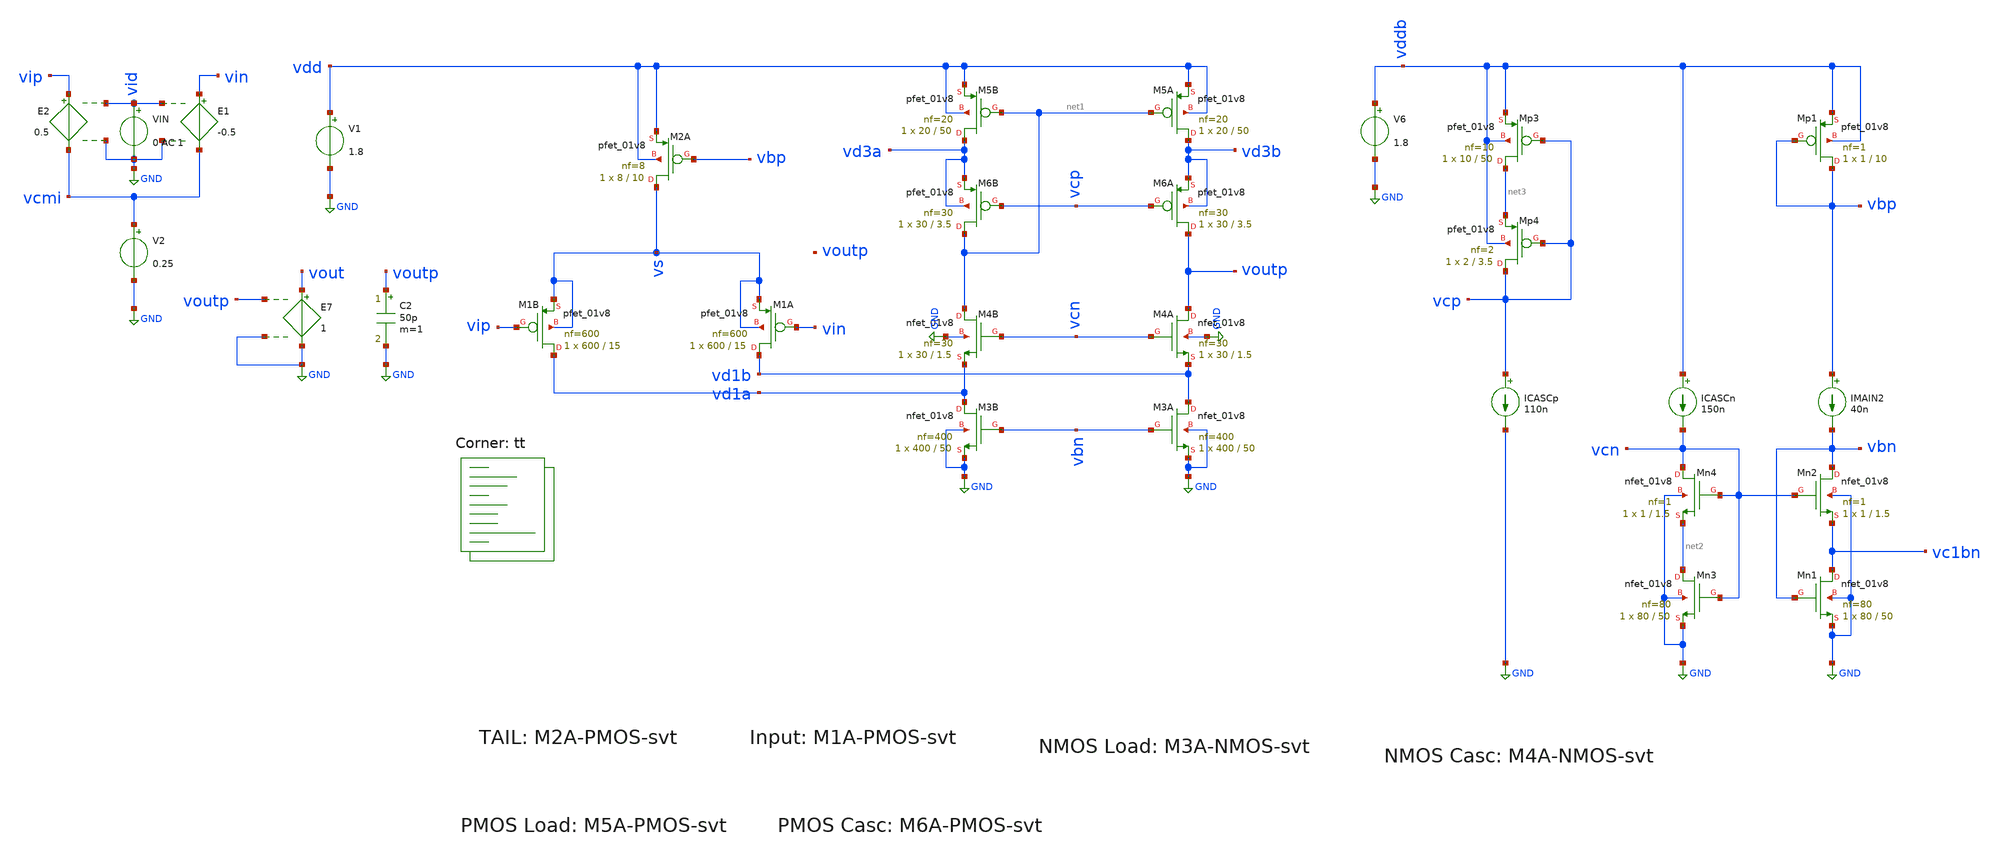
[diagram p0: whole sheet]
** sch_path: circuit-level/xschem/aux-amp/ota_gm_boost_1.sch
**.subckt ota_gm_boost_1
V1 vdd GND 1.8
V2 vcmi GND 0.25
E1 vin vcmi vid GND -0.5
E2 vip vcmi vid GND 0.5
VIN vid GND 0 AC 1
E7 vout GND voutp GND 1
XM2A vs vbp vdd vdd sky130_fd_pr__pfet_01v8 L=10 W=8 nf=8 ad='int((nf+1)/2) * W/nf * 0.29' as='int((nf+2)/2) * W/nf * 0.29'
+ pd='2*int((nf+1)/2) * (W/nf + 0.29)' ps='2*int((nf+2)/2) * (W/nf + 0.29)' nrd='0.29 / W' nrs='0.29 / W'
+ sa=0 sb=0 sd=0 mult=1 m=1
XM1B vd1a vip vs vs sky130_fd_pr__pfet_01v8 L=15 W=600 nf=600 ad='int((nf+1)/2) * W/nf * 0.29' as='int((nf+2)/2) * W/nf * 0.29'
+ pd='2*int((nf+1)/2) * (W/nf + 0.29)' ps='2*int((nf+2)/2) * (W/nf + 0.29)' nrd='0.29 / W' nrs='0.29 / W'
+ sa=0 sb=0 sd=0 mult=1 m=1
XM1A vd1b vin vs vs sky130_fd_pr__pfet_01v8 L=15 W=600 nf=600 ad='int((nf+1)/2) * W/nf * 0.29' as='int((nf+2)/2) * W/nf * 0.29'
+ pd='2*int((nf+1)/2) * (W/nf + 0.29)' ps='2*int((nf+2)/2) * (W/nf + 0.29)' nrd='0.29 / W' nrs='0.29 / W'
+ sa=0 sb=0 sd=0 mult=1 m=1
XM4B net1 vcn vd1a GND sky130_fd_pr__nfet_01v8 L=1.5 W=30 nf=30 ad='int((nf+1)/2) * W/nf * 0.29' as='int((nf+2)/2) * W/nf * 0.29'
+ pd='2*int((nf+1)/2) * (W/nf + 0.29)' ps='2*int((nf+2)/2) * (W/nf + 0.29)' nrd='0.29 / W' nrs='0.29 / W'
+ sa=0 sb=0 sd=0 mult=1 m=1
XM4A voutp vcn vd1b GND sky130_fd_pr__nfet_01v8 L=1.5 W=30 nf=30 ad='int((nf+1)/2) * W/nf * 0.29' as='int((nf+2)/2) * W/nf * 0.29'
+ pd='2*int((nf+1)/2) * (W/nf + 0.29)' ps='2*int((nf+2)/2) * (W/nf + 0.29)' nrd='0.29 / W' nrs='0.29 / W'
+ sa=0 sb=0 sd=0 mult=1 m=1
XM3B vd1a vbn GND GND sky130_fd_pr__nfet_01v8 L=50 W=400 nf=400 ad='int((nf+1)/2) * W/nf * 0.29' as='int((nf+2)/2) * W/nf * 0.29'
+ pd='2*int((nf+1)/2) * (W/nf + 0.29)' ps='2*int((nf+2)/2) * (W/nf + 0.29)' nrd='0.29 / W' nrs='0.29 / W'
+ sa=0 sb=0 sd=0 mult=1 m=1
XM3A vd1b vbn GND GND sky130_fd_pr__nfet_01v8 L=50 W=400 nf=400 ad='int((nf+1)/2) * W/nf * 0.29' as='int((nf+2)/2) * W/nf * 0.29'
+ pd='2*int((nf+1)/2) * (W/nf + 0.29)' ps='2*int((nf+2)/2) * (W/nf + 0.29)' nrd='0.29 / W' nrs='0.29 / W'
+ sa=0 sb=0 sd=0 mult=1 m=1
XM5B vd3a net1 vdd vdd sky130_fd_pr__pfet_01v8 L=50 W=20 nf=20 ad='int((nf+1)/2) * W/nf * 0.29' as='int((nf+2)/2) * W/nf * 0.29'
+ pd='2*int((nf+1)/2) * (W/nf + 0.29)' ps='2*int((nf+2)/2) * (W/nf + 0.29)' nrd='0.29 / W' nrs='0.29 / W'
+ sa=0 sb=0 sd=0 mult=1 m=1
XM5A vd3b net1 vdd vdd sky130_fd_pr__pfet_01v8 L=50 W=20 nf=20 ad='int((nf+1)/2) * W/nf * 0.29' as='int((nf+2)/2) * W/nf * 0.29'
+ pd='2*int((nf+1)/2) * (W/nf + 0.29)' ps='2*int((nf+2)/2) * (W/nf + 0.29)' nrd='0.29 / W' nrs='0.29 / W'
+ sa=0 sb=0 sd=0 mult=1 m=1
C2 voutp GND 50p m=1
XM6B net1 vcp vd3a vd3a sky130_fd_pr__pfet_01v8 L=3.5 W=30 nf=30 ad='int((nf+1)/2) * W/nf * 0.29' as='int((nf+2)/2) * W/nf * 0.29'
+ pd='2*int((nf+1)/2) * (W/nf + 0.29)' ps='2*int((nf+2)/2) * (W/nf + 0.29)' nrd='0.29 / W' nrs='0.29 / W'
+ sa=0 sb=0 sd=0 mult=1 m=1
XM6A voutp vcp vd3b vd3b sky130_fd_pr__pfet_01v8 L=3.5 W=30 nf=30 ad='int((nf+1)/2) * W/nf * 0.29' as='int((nf+2)/2) * W/nf * 0.29'
+ pd='2*int((nf+1)/2) * (W/nf + 0.29)' ps='2*int((nf+2)/2) * (W/nf + 0.29)' nrd='0.29 / W' nrs='0.29 / W'
+ sa=0 sb=0 sd=0 mult=1 m=1
V6 vddb GND 1.8
XMn2 vbn vcn vc1bn GND sky130_fd_pr__nfet_01v8 L=1.5 W=1 nf=1 ad='int((nf+1)/2) * W/nf * 0.29' as='int((nf+2)/2) * W/nf * 0.29'
+ pd='2*int((nf+1)/2) * (W/nf + 0.29)' ps='2*int((nf+2)/2) * (W/nf + 0.29)' nrd='0.29 / W' nrs='0.29 / W'
+ sa=0 sb=0 sd=0 mult=1 m=1
XMn4 vcn vcn net2 GND sky130_fd_pr__nfet_01v8 L=1.5 W=1 nf=1 ad='int((nf+1)/2) * W/nf * 0.29' as='int((nf+2)/2) * W/nf * 0.29'
+ pd='2*int((nf+1)/2) * (W/nf + 0.29)' ps='2*int((nf+2)/2) * (W/nf + 0.29)' nrd='0.29 / W' nrs='0.29 / W'
+ sa=0 sb=0 sd=0 mult=1 m=1
ICASCn vddb vcn 150n
XMn1 vc1bn vbn GND GND sky130_fd_pr__nfet_01v8 L=50 W=80 nf=80 ad='int((nf+1)/2) * W/nf * 0.29' as='int((nf+2)/2) * W/nf * 0.29'
+ pd='2*int((nf+1)/2) * (W/nf + 0.29)' ps='2*int((nf+2)/2) * (W/nf + 0.29)' nrd='0.29 / W' nrs='0.29 / W'
+ sa=0 sb=0 sd=0 mult=1 m=1
IMAIN2 vbp vbn 40n
XMn3 net2 vcn GND GND sky130_fd_pr__nfet_01v8 L=50 W=80 nf=80 ad='int((nf+1)/2) * W/nf * 0.29' as='int((nf+2)/2) * W/nf * 0.29'
+ pd='2*int((nf+1)/2) * (W/nf + 0.29)' ps='2*int((nf+2)/2) * (W/nf + 0.29)' nrd='0.29 / W' nrs='0.29 / W'
+ sa=0 sb=0 sd=0 mult=1 m=1
XMp1 vbp vbp vddb vddb sky130_fd_pr__pfet_01v8 L=10 W=1 nf=1 ad='int((nf+1)/2) * W/nf * 0.29' as='int((nf+2)/2) * W/nf * 0.29'
+ pd='2*int((nf+1)/2) * (W/nf + 0.29)' ps='2*int((nf+2)/2) * (W/nf + 0.29)' nrd='0.29 / W' nrs='0.29 / W'
+ sa=0 sb=0 sd=0 mult=1 m=1
ICASCp vcp GND 110n
XMp3 net3 vcp vddb vddb sky130_fd_pr__pfet_01v8 L=50 W=10 nf=10 ad='int((nf+1)/2) * W/nf * 0.29' as='int((nf+2)/2) * W/nf * 0.29'
+ pd='2*int((nf+1)/2) * (W/nf + 0.29)' ps='2*int((nf+2)/2) * (W/nf + 0.29)' nrd='0.29 / W' nrs='0.29 / W'
+ sa=0 sb=0 sd=0 mult=1 m=1
XMp4 vcp vcp net3 vddb sky130_fd_pr__pfet_01v8 L=3.5 W=2 nf=2 ad='int((nf+1)/2) * W/nf * 0.29' as='int((nf+2)/2) * W/nf * 0.29'
+ pd='2*int((nf+1)/2) * (W/nf + 0.29)' ps='2*int((nf+2)/2) * (W/nf + 0.29)' nrd='0.29 / W' nrs='0.29 / W'
+ sa=0 sb=0 sd=0 mult=1 m=1
**** begin user architecture code
.lib $::SKYWATER_MODELS/sky130.lib.spice tt


.control

save @m.xm1a.msky130_fd_pr__pfet_01v8[id]
save @m.xm1a.msky130_fd_pr__pfet_01v8[vth]
save @m.xm1a.msky130_fd_pr__pfet_01v8[vgs]
save @m.xm1a.msky130_fd_pr__pfet_01v8[vds]
save @m.xm1a.msky130_fd_pr__pfet_01v8[vdsat]
save @m.xm1a.msky130_fd_pr__pfet_01v8[gm]
save @m.xm1a.msky130_fd_pr__pfet_01v8[gds]
save @m.xm1a.msky130_fd_pr__pfet_01v8[cgs]

save @m.xm1b.msky130_fd_pr__pfet_01v8[id]
save @m.xm1b.msky130_fd_pr__pfet_01v8[vth]
save @m.xm1b.msky130_fd_pr__pfet_01v8[vgs]
save @m.xm1b.msky130_fd_pr__pfet_01v8[vds]
save @m.xm1b.msky130_fd_pr__pfet_01v8[vdsat]
save @m.xm1b.msky130_fd_pr__pfet_01v8[gm]
save @m.xm1b.msky130_fd_pr__pfet_01v8[gds]
save @m.xm1b.msky130_fd_pr__pfet_01v8[cgs]

save @m.xm2a.msky130_fd_pr__pfet_01v8[id]
save @m.xm2a.msky130_fd_pr__pfet_01v8[vth]
save @m.xm2a.msky130_fd_pr__pfet_01v8[vgs]
save @m.xm2a.msky130_fd_pr__pfet_01v8[vds]
save @m.xm2a.msky130_fd_pr__pfet_01v8[vdsat]
save @m.xm2a.msky130_fd_pr__pfet_01v8[gm]
save @m.xm2a.msky130_fd_pr__pfet_01v8[gds]
save @m.xm2a.msky130_fd_pr__pfet_01v8[cgs]

save @m.xm5a.msky130_fd_pr__pfet_01v8[id]
save @m.xm5a.msky130_fd_pr__pfet_01v8[vth]
save @m.xm5a.msky130_fd_pr__pfet_01v8[vgs]
save @m.xm5a.msky130_fd_pr__pfet_01v8[vds]
save @m.xm5a.msky130_fd_pr__pfet_01v8[vdsat]
save @m.xm5a.msky130_fd_pr__pfet_01v8[gm]
save @m.xm5a.msky130_fd_pr__pfet_01v8[gds]
save @m.xm5a.msky130_fd_pr__pfet_01v8[cgs]

save @m.xm5b.msky130_fd_pr__pfet_01v8[id]
save @m.xm5b.msky130_fd_pr__pfet_01v8[vth]
save @m.xm5b.msky130_fd_pr__pfet_01v8[vgs]
save @m.xm5b.msky130_fd_pr__pfet_01v8[vds]
save @m.xm5b.msky130_fd_pr__pfet_01v8[vdsat]
save @m.xm5b.msky130_fd_pr__pfet_01v8[gm]
save @m.xm5b.msky130_fd_pr__pfet_01v8[gds]
save @m.xm5b.msky130_fd_pr__pfet_01v8[cgs]

save @m.xm6a.msky130_fd_pr__pfet_01v8[id]
save @m.xm6a.msky130_fd_pr__pfet_01v8[vth]
save @m.xm6a.msky130_fd_pr__pfet_01v8[vgs]
save @m.xm6a.msky130_fd_pr__pfet_01v8[vds]
save @m.xm6a.msky130_fd_pr__pfet_01v8[vdsat]
save @m.xm6a.msky130_fd_pr__pfet_01v8[gm]
save @m.xm6a.msky130_fd_pr__pfet_01v8[gds]
save @m.xm6a.msky130_fd_pr__pfet_01v8[cgs]

save @m.xm6b.msky130_fd_pr__pfet_01v8[id]
save @m.xm6b.msky130_fd_pr__pfet_01v8[vth]
save @m.xm6b.msky130_fd_pr__pfet_01v8[vgs]
save @m.xm6b.msky130_fd_pr__pfet_01v8[vds]
save @m.xm6b.msky130_fd_pr__pfet_01v8[vdsat]
save @m.xm6b.msky130_fd_pr__pfet_01v8[gm]
save @m.xm6b.msky130_fd_pr__pfet_01v8[gds]
save @m.xm6b.msky130_fd_pr__pfet_01v8[cgs]


.endc



.control

save @m.xm3a.msky130_fd_pr__nfet_01v8[id]
save @m.xm3a.msky130_fd_pr__nfet_01v8[vth]
save @m.xm3a.msky130_fd_pr__nfet_01v8[vgs]
save @m.xm3a.msky130_fd_pr__nfet_01v8[vds]
save @m.xm3a.msky130_fd_pr__nfet_01v8[vdsat]
save @m.xm3a.msky130_fd_pr__nfet_01v8[gm]
save @m.xm3a.msky130_fd_pr__nfet_01v8[gds]
save @m.xm3a.msky130_fd_pr__nfet_01v8[cgs]

save @m.xm3b.msky130_fd_pr__nfet_01v8[id]
save @m.xm3b.msky130_fd_pr__nfet_01v8[vth]
save @m.xm3b.msky130_fd_pr__nfet_01v8[vgs]
save @m.xm3b.msky130_fd_pr__nfet_01v8[vds]
save @m.xm3b.msky130_fd_pr__nfet_01v8[vdsat]
save @m.xm3b.msky130_fd_pr__nfet_01v8[gm]
save @m.xm3b.msky130_fd_pr__nfet_01v8[gds]
save @m.xm3b.msky130_fd_pr__nfet_01v8[cgs]

save @m.xm4a.msky130_fd_pr__nfet_01v8[id]
save @m.xm4a.msky130_fd_pr__nfet_01v8[vth]
save @m.xm4a.msky130_fd_pr__nfet_01v8[vgs]
save @m.xm4a.msky130_fd_pr__nfet_01v8[vds]
save @m.xm4a.msky130_fd_pr__nfet_01v8[vdsat]
save @m.xm4a.msky130_fd_pr__nfet_01v8[gm]
save @m.xm4a.msky130_fd_pr__nfet_01v8[gds]
save @m.xm4a.msky130_fd_pr__nfet_01v8[cgs]

save @m.xm4b.msky130_fd_pr__nfet_01v8[id]
save @m.xm4b.msky130_fd_pr__nfet_01v8[vth]
save @m.xm4b.msky130_fd_pr__nfet_01v8[vgs]
save @m.xm4b.msky130_fd_pr__nfet_01v8[vds]
save @m.xm4b.msky130_fd_pr__nfet_01v8[vdsat]
save @m.xm4b.msky130_fd_pr__nfet_01v8[gm]
save @m.xm4b.msky130_fd_pr__nfet_01v8[gds]
save @m.xm4b.msky130_fd_pr__nfet_01v8[cgs]


.endc



.options savecurrents
.control
save all

let tr = 20u
let tf = 1u
let tper = 1
let tpulse = 200u
let tdelay1 = 100n
alter @VIN[PULSE]=[ 0 0.5 $&tdelay1 $&tr $&tf $&tpulse $&tper 0 ]

set wr_singlescale
set wr_vecnames
option numdgt=5


** Main Simulations

	*dc VIN -0.81 0.81 0.008
	ac dec 100 0.1 1e5
	noise v(vout) VIN dec 100 0.1 100k 1
	noise v(vout) VIN dec 10 0.1 128
	alter @V2[DC] = 0
	tran 50n 100u

	setplot noise1
	let acGain = onoise_spectrum/inoise_spectrum
	let m1_in = onoise.m.xm1a.msky130_fd_pr__pfet_01v8/acGain
	let m2_in = onoise.m.xm2a.msky130_fd_pr__pfet_01v8/acGain
	let m3_in = onoise.m.xm3a.msky130_fd_pr__nfet_01v8/acGain
	let m4_in = onoise.m.xm4a.msky130_fd_pr__nfet_01v8/acGain
	let m5_in = onoise.m.xm5a.msky130_fd_pr__pfet_01v8/acGain
	let m6_in = onoise.m.xm6a.msky130_fd_pr__pfet_01v8/acGain
	plot inoise_spectrum m1_in m2_in m3_in m4_in m5_in m6_in
	*plot inoise_spectrum
	*plot onoise_spectrum

	setplot ac1
	let A = v(vout)/v(vin)
	let Amag_dB = vdb(A)
	let Aarg = 180/PI*cphase(A)
	plot Amag_dB Aarg
	meas ac Adc max Amag_dB
	let Amag_dB_3dB = Adc-3
	meas ac f3db find frequency when Amag_dB=Amag_dB_3dB
	meas ac fug find frequency when Amag_dB=0
	meas ac arg_fug find Aarg when frequency=fug
	let pm = 180-abs(arg_fug)
	wrdata /foss/designs/frontend/auxamp_ac.txt Amag_dB Aarg
	setplot tran4
	plot v(voutp) v(vip)



op
let gmId1 = @m.xm1a.msky130_fd_pr__pfet_01v8[gm]/@m.xm1a.msky130_fd_pr__pfet_01v8[id]
let gmId2 = @m.xm2a.msky130_fd_pr__pfet_01v8[gm]/@m.xm2a.msky130_fd_pr__pfet_01v8[id]
let gmId3 = @m.xm3a.msky130_fd_pr__nfet_01v8[gm]/@m.xm3a.msky130_fd_pr__nfet_01v8[id]
let gmId4 = @m.xm4a.msky130_fd_pr__nfet_01v8[gm]/@m.xm4a.msky130_fd_pr__nfet_01v8[id]
let gmId5 = @m.xm5a.msky130_fd_pr__pfet_01v8[gm]/@m.xm5a.msky130_fd_pr__pfet_01v8[id]
let gmId6 = @m.xm5a.msky130_fd_pr__pfet_01v8[gm]/@m.xm6a.msky130_fd_pr__pfet_01v8[id]

let rout_m4a =
+ @m.xm4a.msky130_fd_pr__nfet_01v8[gm]*(1/(@m.xm1a.msky130_fd_pr__pfet_01v8[gds]+@m.xm3a.msky130_fd_pr__nfet_01v8[gds]))/@m.xm4a.msky130_fd_pr__nfet_01v8[gds]
let rout_m6a =
+ @m.xm6a.msky130_fd_pr__pfet_01v8[gm]/@m.xm5a.msky130_fd_pr__pfet_01v8[gds]/@m.xm6a.msky130_fd_pr__pfet_01v8[gds]
let rout = 1/(1/rout_m4a+1/rout_m6a)
let A0 = rout*@m.xm1a.msky130_fd_pr__pfet_01v8[gm]
remzerovec
write ota_gm_boost_1.raw
.endc

**** end user architecture code
**.ends
.GLOBAL GND
.end
